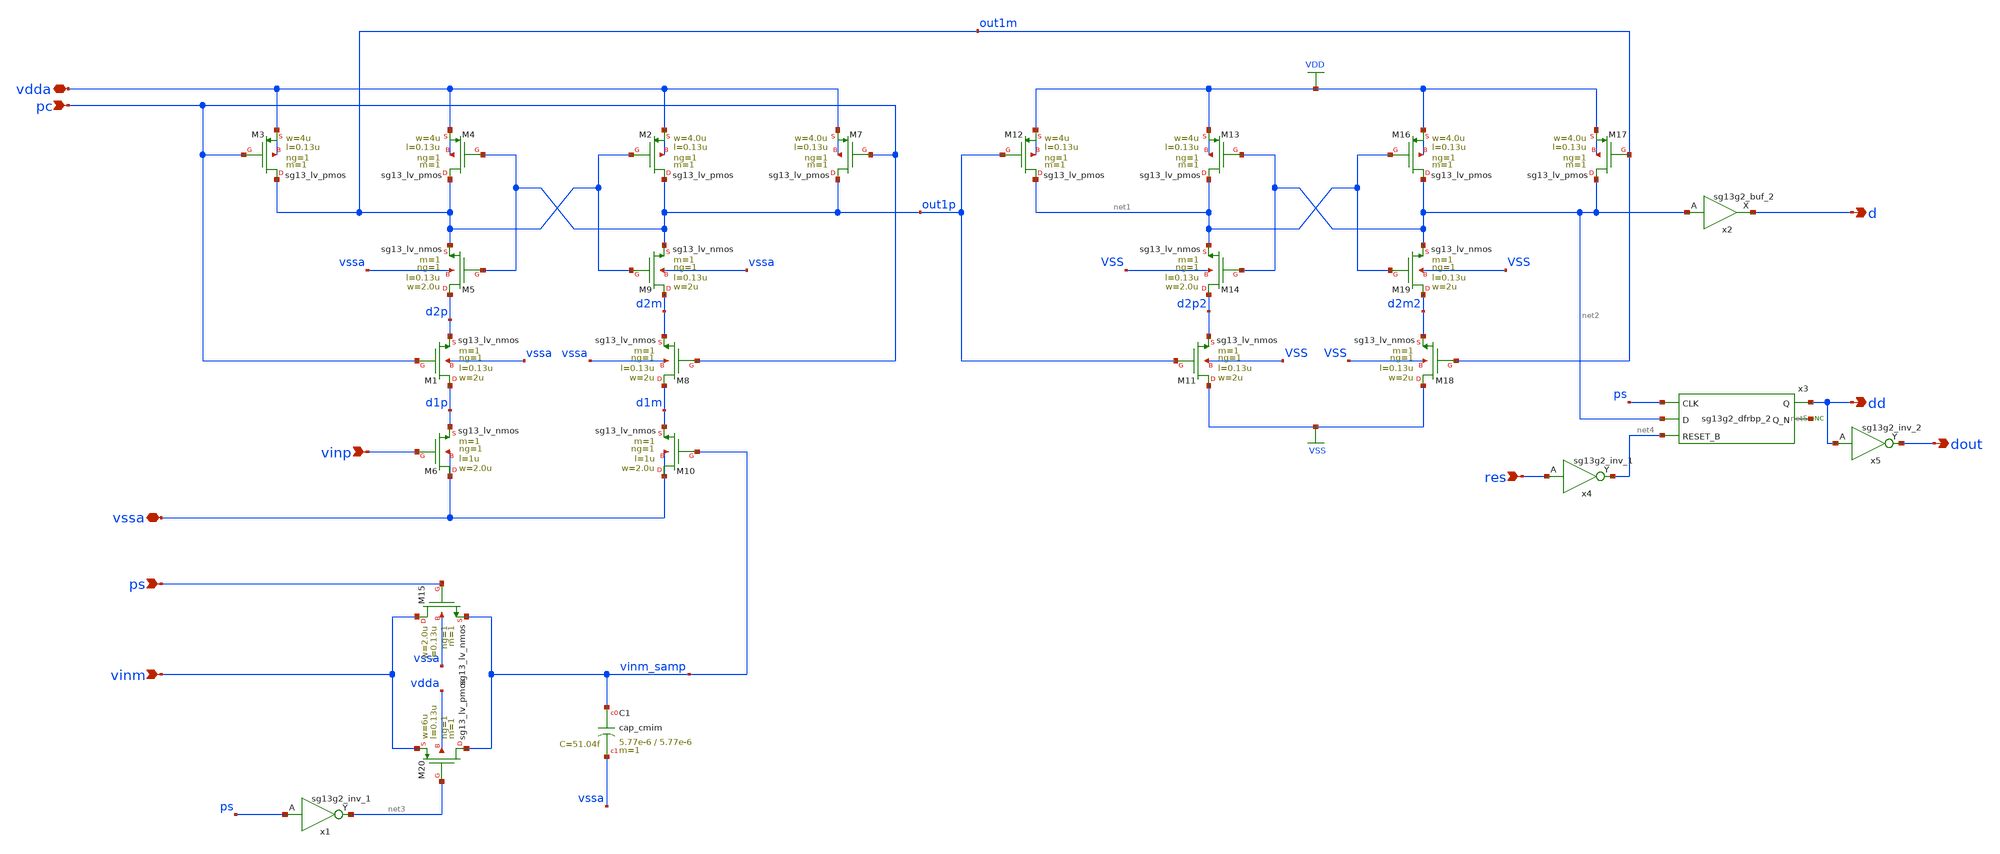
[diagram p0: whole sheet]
** sch_path: 5_Design/4_Layout/Team 2 - Transformer Monster Tractors/xschem/comparator_latch_T2.sch
* Copyright 2023  IHP PDK Authors
* Licensed under the Apache License, Version 2.0 (the "License");
* you may not use this file except in compliance with the License.
* You may obtain a copy of the License at
* https://www.apache.org/licenses/LICENSE-2.0
* Unless required by applicable law or agreed to in writing, software
* distributed under the License is distributed on an "AS IS" BASIS,
* WITHOUT WARRANTIES OR CONDITIONS OF ANY KIND, either express or implied.
* See the License for the specific language governing permissions and
* limitations under the License.
**.subckt comparator_latch_T2 vdda vssa pc vinp vinm ps dd d res dout
*.iopin vdda
*.iopin vssa
*.ipin pc
*.ipin vinp
*.ipin vinm
*.ipin ps
*.opin dd
*.opin d
*.ipin res
*.opin dout
XM1 d1p pc d2p vssa sg13_lv_nmos w=2u l=0.13u ng=1 m=1 mm_ok=1
XM3 out1m pc vdda vdda sg13_lv_pmos w=4u l=0.13u ng=1 m=1 mm_ok=1
XM4 out1m out1p vdda vdda sg13_lv_pmos w=4u l=0.13u ng=1 m=1 mm_ok=1
XM5 d2p out1p out1m vssa sg13_lv_nmos w=2.0u l=0.13u ng=1 m=1 mm_ok=1
XM6 vssa vinp d1p vssa sg13_lv_nmos w=2.0u l=1u ng=1 m=1 mm_ok=1
XM2 out1p out1m vdda vdda sg13_lv_pmos w=4.0u l=0.13u ng=1 m=1 mm_ok=1
XM7 out1p pc vdda vdda sg13_lv_pmos w=4.0u l=0.13u ng=1 m=1 mm_ok=1
XM8 d1m pc d2m vssa sg13_lv_nmos w=2u l=0.13u ng=1 m=1 mm_ok=1
XM9 d2m out1m out1p vssa sg13_lv_nmos w=2u l=0.13u ng=1 m=1 mm_ok=1
XM10 vssa vinm_samp d1m vssa sg13_lv_nmos w=2.0u l=1u ng=1 m=1 mm_ok=1
XM11 VSS out1p d2p2 VSS sg13_lv_nmos w=2u l=0.13u ng=1 m=1 mm_ok=1
XM12 net1 out1p VDD VDD sg13_lv_pmos w=4u l=0.13u ng=1 m=1 mm_ok=1
XM13 net1 net2 VDD VDD sg13_lv_pmos w=4u l=0.13u ng=1 m=1 mm_ok=1
XM14 d2p2 net2 net1 VSS sg13_lv_nmos w=2.0u l=0.13u ng=1 m=1 mm_ok=1
XM16 net2 net1 VDD VDD sg13_lv_pmos w=4.0u l=0.13u ng=1 m=1 mm_ok=1
XM17 net2 out1m VDD VDD sg13_lv_pmos w=4.0u l=0.13u ng=1 m=1 mm_ok=1
XM18 VSS out1m d2m2 VSS sg13_lv_nmos w=2u l=0.13u ng=1 m=1 mm_ok=1
XM19 d2m2 net1 net2 VSS sg13_lv_nmos w=2u l=0.13u ng=1 m=1 mm_ok=1
XM15 vinm ps vinm_samp vssa sg13_lv_nmos w=2.0u l=0.13u ng=1 m=1 mm_ok=1
XM20 vinm_samp net3 vinm vdda sg13_lv_pmos w=6u l=0.13u ng=1 m=1 mm_ok=1
x1 net3 ps VDD VSS sg13g2_inv_1
x2 d net2 VDD VSS sg13g2_buf_2
x3 dd net5 ps net2 net4 VDD VSS sg13g2_dfrbp_2
x4 net4 res VDD VSS sg13g2_inv_1
XC1 vinm_samp vssa cap_cmim w=5.77e-6 l=5.77e-6 m=1 mm_ok=1
x5 dout dd VDD VSS sg13g2_inv_2
* noconn #net5
**.ends

* expanding   symbol:  sg13g2_stdcells/sg13g2_inv_1.sym # of pins=2
** sym_path: sg13g2_stdcells/sg13g2_inv_1.sym
** sch_path: sg13g2_stdcells/sg13g2_inv_1.sch
.subckt sg13g2_inv_1 Y A VDD VSS
*.opin Y
*.ipin A
*.iopin VDD
*.iopin VSS
XM1 Y A VSS VSS sg13_lv_nmos w=740.00n l=130.00n ng=1 m=1 mm_ok=1
XM2 Y A VDD VDD sg13_lv_pmos w=1.12u l=130.00n ng=1 m=1 mm_ok=1
.ends


* expanding   symbol:  sg13g2_stdcells/sg13g2_buf_2.sym # of pins=2
** sym_path: sg13g2_stdcells/sg13g2_buf_2.sym
** sch_path: sg13g2_stdcells/sg13g2_buf_2.sch
.subckt sg13g2_buf_2 X A VDD VSS
*.ipin A
*.opin X
*.iopin VDD
*.iopin VSS
XM1 net1 A VSS VSS sg13_lv_nmos w=640.00n l=130.00n ng=1 m=1 mm_ok=1
XM2 X net1 VSS VSS sg13_lv_nmos w=1.48u l=130.00n ng=2 m=1 mm_ok=1
XM3 net1 A VDD VDD sg13_lv_pmos w=1.000u l=130.00n ng=1 m=1 mm_ok=1
XM4 X net1 VDD VDD sg13_lv_pmos w=2.24u l=130.00n ng=2 m=1 mm_ok=1
.ends


* expanding   symbol:  sg13g2_stdcells/sg13g2_dfrbp_2.sym # of pins=5
** sym_path: sg13g2_stdcells/sg13g2_dfrbp_2.sym
** sch_path: sg13g2_stdcells/sg13g2_dfrbp_2.sch
.subckt sg13g2_dfrbp_2 Q Q_N CLK D RESET_B VDD VSS
*.ipin D
*.ipin RESET_B
*.ipin CLK
*.opin Q
*.opin Q_N
*.iopin VDD
*.iopin VSS
XM1 Db D net12 VSS sg13_lv_nmos w=420.00n l=130.00n ng=1 m=1 mm_ok=1
XM2 net12 RESET_B VSS VSS sg13_lv_nmos w=420.00n l=130.00n ng=1 m=1 mm_ok=1
XM3 net2 clkneg net11 VSS sg13_lv_nmos w=420.00n l=130.00n ng=1 m=1 mm_ok=1
XM4 net11 net3 VSS VSS sg13_lv_nmos w=420.00n l=130.00n ng=1 m=1 mm_ok=1
XM5 net3 net2 net7 VSS sg13_lv_nmos w=420.00n l=130.00n ng=1 m=1 mm_ok=1
XM6 net7 RESET_B VSS VSS sg13_lv_nmos w=420.00n l=130.00n ng=1 m=1 mm_ok=1
XM7 Q_N net2 VSS VSS sg13_lv_nmos w=1.48u l=130.00n ng=2 m=1 mm_ok=1
XM8 net1 net2 VSS VSS sg13_lv_nmos w=640.00n l=130.00n ng=1 m=1 mm_ok=1
XM9 Q net1 VSS VSS sg13_lv_nmos w=1.48u l=130.00n ng=2 m=1 mm_ok=1
XM10 clkneg CLK VSS VSS sg13_lv_nmos w=740.00n l=130.00n ng=1 m=1 mm_ok=1
XM11 clkpos clkneg VSS VSS sg13_lv_nmos w=740.00n l=130.00n ng=1 m=1 mm_ok=1
XM12 Db clkneg net4 VSS sg13_lv_nmos w=420.00n l=130.00n ng=1 m=1 mm_ok=1
XM13 net4 clkpos net10 VSS sg13_lv_nmos w=420.00n l=130.00n ng=1 m=1 mm_ok=1
XM14 net10 net5 net6 VSS sg13_lv_nmos w=420.00n l=130.00n ng=1 m=1 mm_ok=1
XM15 net6 RESET_B VSS VSS sg13_lv_nmos w=420.00n l=130.00n ng=1 m=1 mm_ok=1
XM16 net5 net4 VSS VSS sg13_lv_nmos w=740.00n l=130.00n ng=1 m=1 mm_ok=1
XM17 net5 clkpos net2 VSS sg13_lv_nmos w=740.00n l=130.00n ng=1 m=1 mm_ok=1
XM18 Db RESET_B VDD VDD sg13_lv_pmos w=420.00n l=130.00n ng=1 m=1 mm_ok=1
XM19 Db D VDD VDD sg13_lv_pmos w=420.00n l=130.00n ng=1 m=1 mm_ok=1
XM20 net9 net3 VDD VDD sg13_lv_pmos w=420.00n l=130.00n ng=1 m=1 mm_ok=1
XM21 net2 clkpos net9 VDD sg13_lv_pmos w=420.00n l=130.00n ng=1 m=1 mm_ok=1
XM22 net3 net2 VDD VDD sg13_lv_pmos w=420.00n l=130.00n ng=1 m=1 mm_ok=1
XM23 net3 RESET_B VDD VDD sg13_lv_pmos w=420.00n l=130.00n ng=1 m=1 mm_ok=1
XM24 Q_N net2 VDD VDD sg13_lv_pmos w=2.24u l=130.00n ng=2 m=1 mm_ok=1
XM25 net1 net2 VDD VDD sg13_lv_pmos w=1.000u l=130.00n ng=1 m=1 mm_ok=1
XM26 Q net1 VDD VDD sg13_lv_pmos w=2.24u l=130.00n ng=2 m=1 mm_ok=1
XM27 clkneg CLK VDD VDD sg13_lv_pmos w=1.12u l=130.00n ng=1 m=1 mm_ok=1
XM28 clkpos clkneg VDD VDD sg13_lv_pmos w=1.12u l=130.00n ng=1 m=1 mm_ok=1
XM29 Db clkpos net4 VDD sg13_lv_pmos w=420.00n l=130.00n ng=1 m=1 mm_ok=1
XM30 net8 net5 VDD VDD sg13_lv_pmos w=420.00n l=130.00n ng=1 m=1 mm_ok=1
XM31 net4 clkneg net8 VDD sg13_lv_pmos w=420.00n l=130.00n ng=1 m=1 mm_ok=1
XM32 net4 RESET_B VDD VDD sg13_lv_pmos w=420.00n l=130.00n ng=1 m=1 mm_ok=1
XM33 net5 net4 VDD VDD sg13_lv_pmos w=1.000u l=130.00n ng=1 m=1 mm_ok=1
XM34 net5 clkneg net2 VDD sg13_lv_pmos w=1.000u l=130.00n ng=1 m=1 mm_ok=1
.ends


* expanding   symbol:  sg13g2_stdcells/sg13g2_inv_2.sym # of pins=2
** sym_path: sg13g2_stdcells/sg13g2_inv_2.sym
** sch_path: sg13g2_stdcells/sg13g2_inv_2.sch
.subckt sg13g2_inv_2 Y A VDD VSS
*.opin Y
*.ipin A
*.iopin VDD
*.iopin VSS
XM1 Y A VSS VSS sg13_lv_nmos w=1.48u l=130.00n ng=2 m=1 mm_ok=1
XM2 Y A VDD VDD sg13_lv_pmos w=2.24u l=130.00n ng=2 m=1 mm_ok=1
.ends

.GLOBAL VDD
.GLOBAL VSS
.end
